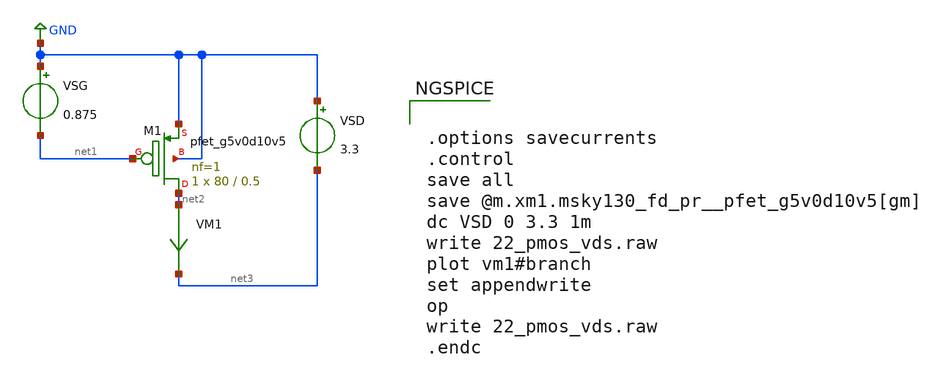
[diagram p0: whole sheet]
** sch_path: xschem/help/22_pmos_vds.sch
**.subckt 22_pmos_vds
VSG GND net1 0.875
VSD GND net3 3.3
VM1 net2 net3 0
.save i(vm1)
XM1 net2 net1 GND GND sky130_fd_pr__pfet_g5v0d10v5 L=0.5 W=80 nf=1 ad='int((nf+1)/2) * W/nf * 0.29' as='int((nf+2)/2) * W/nf * 0.29'
+ pd='2*int((nf+1)/2) * (W/nf + 0.29)' ps='2*int((nf+2)/2) * (W/nf + 0.29)' nrd='0.29 / W' nrs='0.29 / W'
+ sa=0 sb=0 sd=0 mult=1 m=1
**** begin user architecture code


.options savecurrents
.control
save all
save @m.xm1.msky130_fd_pr__pfet_g5v0d10v5[gm]
dc VSD 0 3.3 1m
write 22_pmos_vds.raw
plot vm1#branch
set appendwrite
op
write 22_pmos_vds.raw
.endc



** opencircuitdesign pdks install
.lib $::SKYWATER_MODELS/sky130.lib.spice tt


**** end user architecture code
**.ends
.GLOBAL GND
.end
